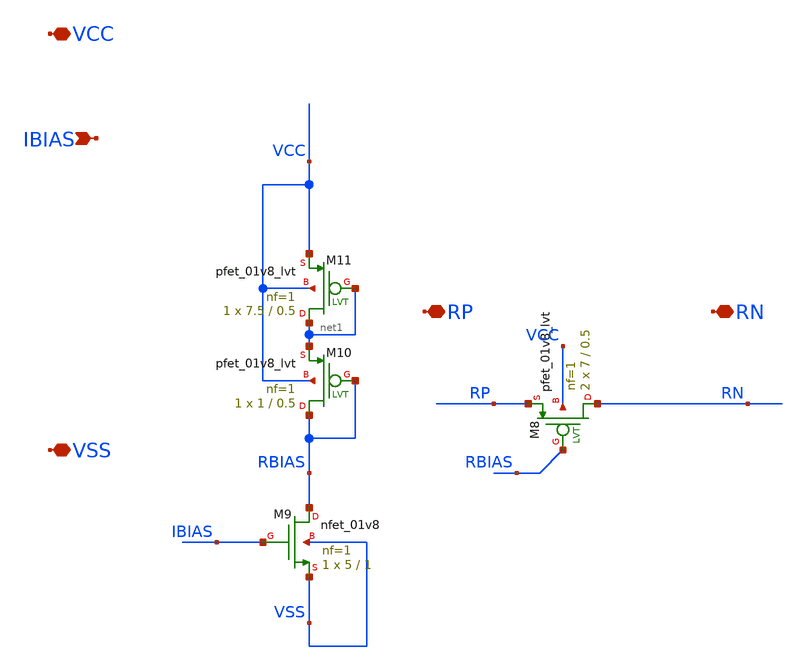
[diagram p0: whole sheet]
** sch_path: xschem/active-resistor.sch
**.subckt active-resistor VCC VSS IBIAS RP RN
*.iopin VCC
*.iopin VSS
*.ipin IBIAS
*.iopin RP
*.iopin RN
XM9 RBIAS IBIAS VSS VSS sky130_fd_pr__nfet_01v8 L=1 W=5 nf=1 ad='int((nf+1)/2) * W/nf * 0.29' as='int((nf+2)/2) * W/nf * 0.29'
+ pd='2*int((nf+1)/2) * (W/nf + 0.29)' ps='2*int((nf+2)/2) * (W/nf + 0.29)' nrd='0.29 / W' nrs='0.29 / W'
+ sa=0 sb=0 sd=0 mult=1 m=1
XM10 RBIAS RBIAS net1 VCC sky130_fd_pr__pfet_01v8_lvt L=0.5 W=1 nf=1 ad='int((nf+1)/2) * W/nf * 0.29'
+ as='int((nf+2)/2) * W/nf * 0.29' pd='2*int((nf+1)/2) * (W/nf + 0.29)' ps='2*int((nf+2)/2) * (W/nf + 0.29)'
+ nrd='0.29 / W' nrs='0.29 / W' sa=0 sb=0 sd=0 mult=1 m=1
XM11 net1 net1 VCC VCC sky130_fd_pr__pfet_01v8_lvt L=0.5 W=7.5 nf=1 ad='int((nf+1)/2) * W/nf * 0.29'
+ as='int((nf+2)/2) * W/nf * 0.29' pd='2*int((nf+1)/2) * (W/nf + 0.29)' ps='2*int((nf+2)/2) * (W/nf + 0.29)'
+ nrd='0.29 / W' nrs='0.29 / W' sa=0 sb=0 sd=0 mult=1 m=1
XM8 RN RBIAS RP VCC sky130_fd_pr__pfet_01v8_lvt L=0.5 W=7 nf=1 ad='int((nf+1)/2) * W/nf * 0.29' as='int((nf+2)/2) * W/nf * 0.29'
+ pd='2*int((nf+1)/2) * (W/nf + 0.29)' ps='2*int((nf+2)/2) * (W/nf + 0.29)' nrd='0.29 / W' nrs='0.29 / W'
+ sa=0 sb=0 sd=0 mult=2 m=2
**.ends
.end
